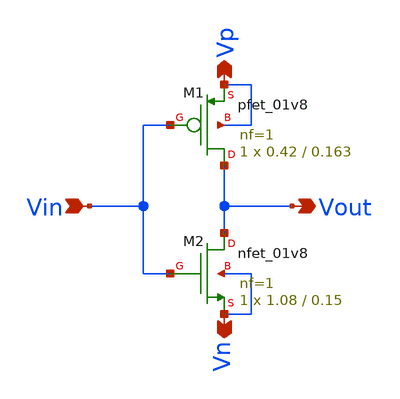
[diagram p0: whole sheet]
** sch_path: xschem/Vth_sch/Symbol/Inverter-th07.sch
**.subckt Inverter-th07 Vin Vout Vp Vn
*.ipin Vin
*.opin Vout
*.opin Vp
*.opin Vn
XM1 Vout Vin Vp Vp sky130_fd_pr__pfet_01v8 L=0.163 W=0.42 nf=1 ad='int((nf+1)/2) * W/nf * 0.29' as='int((nf+2)/2) * W/nf * 0.29'
+ pd='2*int((nf+1)/2) * (W/nf + 0.29)' ps='2*int((nf+2)/2) * (W/nf + 0.29)' nrd='0.29 / W' nrs='0.29 / W'
+ sa=0 sb=0 sd=0 mult=1 m=1
XM2 Vout Vin Vn Vn sky130_fd_pr__nfet_01v8 L=0.15 W=1.08 nf=1 ad='int((nf+1)/2) * W/nf * 0.29' as='int((nf+2)/2) * W/nf * 0.29'
+ pd='2*int((nf+1)/2) * (W/nf + 0.29)' ps='2*int((nf+2)/2) * (W/nf + 0.29)' nrd='0.29 / W' nrs='0.29 / W'
+ sa=0 sb=0 sd=0 mult=1 m=1
**.ends
.end
